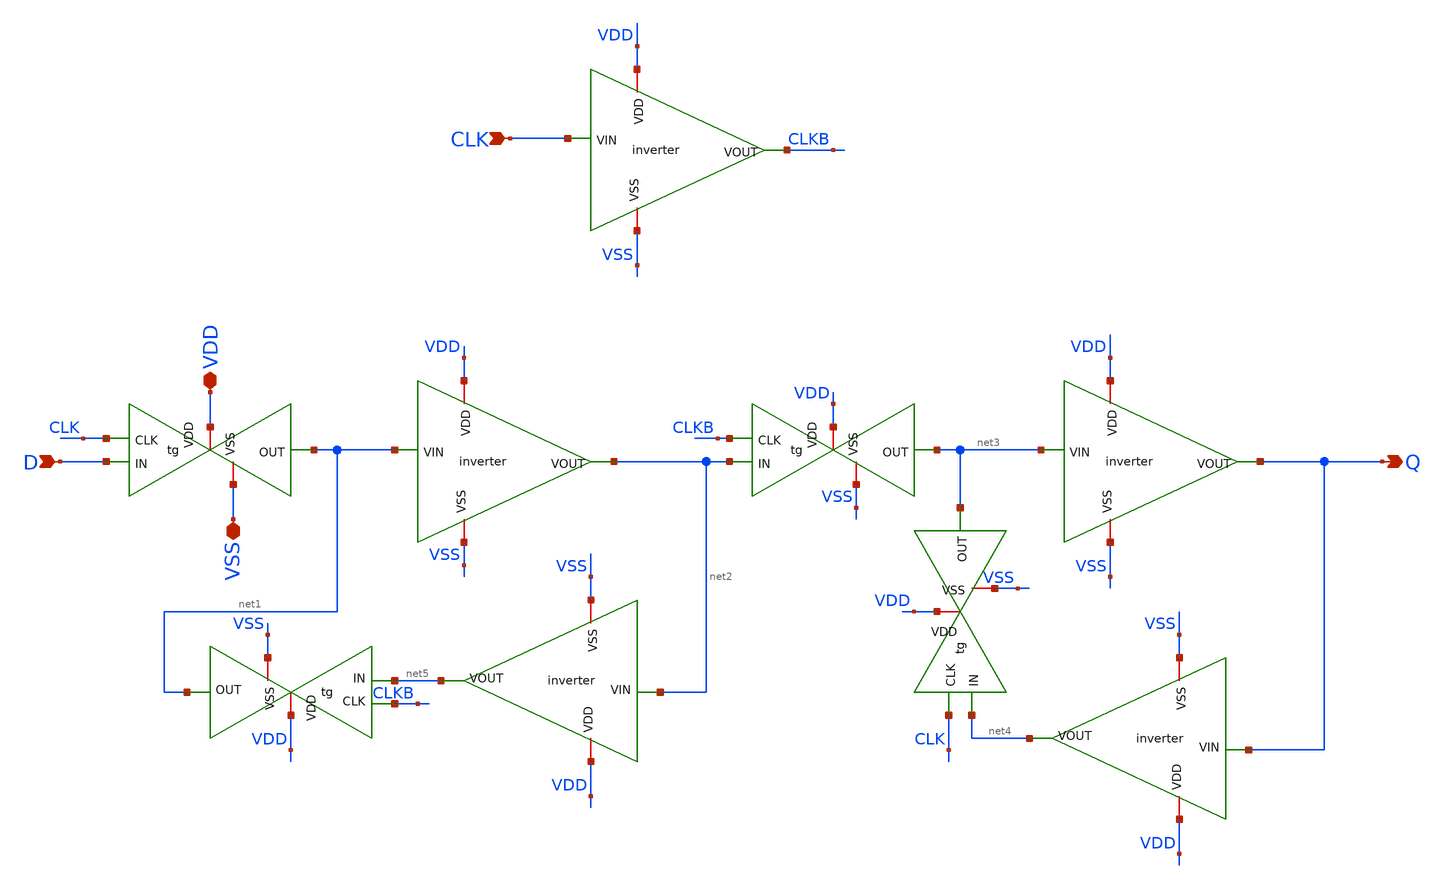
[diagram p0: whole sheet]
** sch_path: Xschem/PLL_TOP_Schematics/ned_DFF.sch
* Xschem/PLL_TOP_Schematics/inverter.sch:
* Copyright 2022 GlobalFoundries PDK Authors
* Licensed under the Apache License, Version 2.0 (the "License");
**.subckt ned_DFF D VDD VSS Q CLK
*.ipin D
*.iopin VDD
*.iopin VSS
*.opin Q
*.ipin CLK
x1 VDD CLK VSS net1 D tg
x3 VDD CLKB VSS net3 net2 tg
x4 VDD CLKB VSS net1 net5 tg
x5 VDD CLK VSS net3 net4 tg
x2 VDD CLK CLKB VSS inverter
x6 VDD net1 net2 VSS inverter
x7 VDD net2 net5 VSS inverter
x8 VDD Q net4 VSS inverter
x9 VDD net3 Q VSS inverter
**.ends

* expanding   symbol:  tg.sym # of pins=5
** sym_path: Xschem/PLL_TOP_Schematics/tg.sym
** sch_path: Xschem/PLL_TOP_Schematics/tg.sch
.subckt tg VDD CLK VSS OUT IN
*.iopin VDD
*.iopin VSS
*.ipin CLK
*.ipin IN
*.opin OUT
x1 VDD CLK net1 VSS inverter
XM5 OUT net1 IN VDD sky130_fd_pr__pfet_01v8 L=0.2 W=3.5 nf=1 ad='int((nf+1)/2) * W/nf * 0.29' as='int((nf+2)/2) * W/nf * 0.29'
+ pd='2*int((nf+1)/2) * (W/nf + 0.29)' ps='2*int((nf+2)/2) * (W/nf + 0.29)' nrd='0.29 / W' nrs='0.29 / W'
+ sa=0 sb=0 sd=0 mult=1 m=1
XM2 OUT CLK IN VSS sky130_fd_pr__nfet_01v8 L=0.2 W=3.5 nf=1 ad='int((nf+1)/2) * W/nf * 0.29' as='int((nf+2)/2) * W/nf * 0.29'
+ pd='2*int((nf+1)/2) * (W/nf + 0.29)' ps='2*int((nf+2)/2) * (W/nf + 0.29)' nrd='0.29 / W' nrs='0.29 / W'
+ sa=0 sb=0 sd=0 mult=1 m=1
.ends


* expanding   symbol:  inverter.sym # of pins=4
** sym_path: Xschem/PLL_TOP_Schematics/inverter.sym
** sch_path: Xschem/PLL_TOP_Schematics/inverter.sch
.subckt inverter VDD VIN VOUT VSS
*.iopin VDD
*.ipin VIN
*.opin VOUT
*.iopin VSS
XM5 VOUT VIN VDD VDD sky130_fd_pr__pfet_01v8 L=0.2 W=5 nf=1 ad='int((nf+1)/2) * W/nf * 0.29' as='int((nf+2)/2) * W/nf * 0.29'
+ pd='2*int((nf+1)/2) * (W/nf + 0.29)' ps='2*int((nf+2)/2) * (W/nf + 0.29)' nrd='0.29 / W' nrs='0.29 / W'
+ sa=0 sb=0 sd=0 mult=1 m=1
XM1 VOUT VIN VSS VSS sky130_fd_pr__nfet_01v8 L=0.2 W=2.5 nf=1 ad='int((nf+1)/2) * W/nf * 0.29' as='int((nf+2)/2) * W/nf * 0.29'
+ pd='2*int((nf+1)/2) * (W/nf + 0.29)' ps='2*int((nf+2)/2) * (W/nf + 0.29)' nrd='0.29 / W' nrs='0.29 / W'
+ sa=0 sb=0 sd=0 mult=1 m=1
.ends

.end
